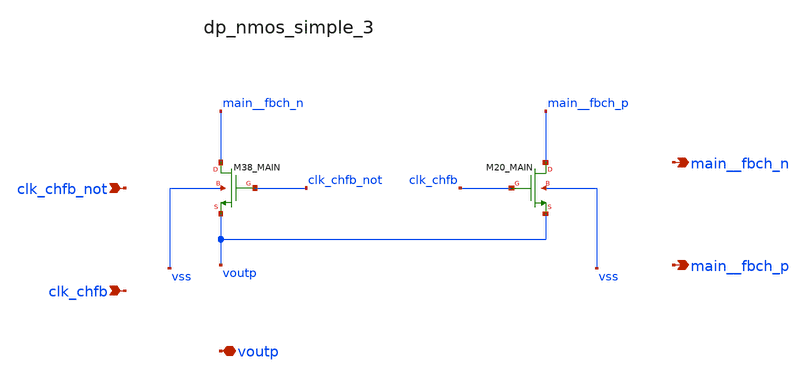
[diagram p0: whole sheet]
** sch_path: analog-db/raw/ia_004_fan_chopper_rrl/hier/blocks/dp_nmos_simple_3.sch
**.subckt dp_nmos_simple_3 clk_chfb_not clk_chfb voutp main__fbch_n main__fbch_p
*.ipin clk_chfb_not
*.ipin clk_chfb
*.iopin voutp
*.opin main__fbch_n
*.opin main__fbch_p
XM20_MAIN main__fbch_p clk_chfb voutp vss sg13_lv_nmos w=x_dut_xm20_main_w l=x_dut_xm20_main_l ng=1
+ m=x_dut_xm20_main_m
XM38_MAIN main__fbch_n clk_chfb_not voutp vss sg13_lv_nmos w=x_dut_xm38_main_w l=x_dut_xm38_main_l
+ ng=1 m=x_dut_xm38_main_m
**.ends
.end
